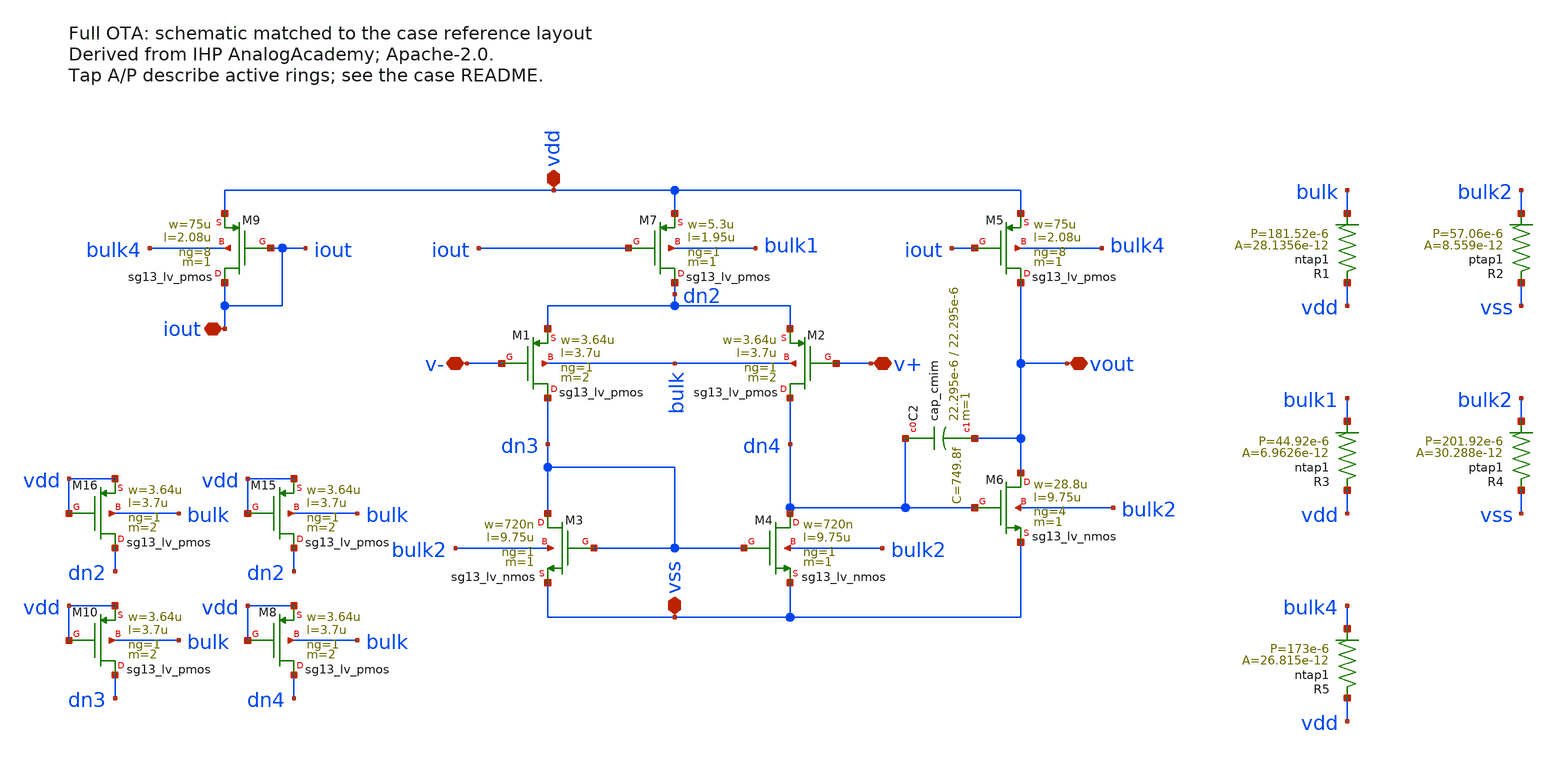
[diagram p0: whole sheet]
** sch_path: tasks/IHP-AnalogAcademy/cases/full_OTA/source/two_stage_OTA_layout.sch
**.subckt two_stage_OTA_layout v- v+ vss vdd iout vout
*.iopin v-
*.iopin v+
*.iopin vss
*.iopin vdd
*.iopin iout
*.iopin vout
XM4 dn4 dn3 vss bulk2 sg13_lv_nmos w=720n l=9.75u ng=1 m=1 mm_ok=1
XM3 dn3 dn3 vss bulk2 sg13_lv_nmos w=720n l=9.75u ng=1 m=1 mm_ok=1
XM1 dn3 v- dn2 bulk sg13_lv_pmos w=3.64u l=3.7u ng=1 m=2 mm_ok=1
XM2 dn4 v+ dn2 bulk sg13_lv_pmos w=3.64u l=3.7u ng=1 m=2 mm_ok=1
XM7 dn2 iout vdd bulk1 sg13_lv_pmos w=5.3u l=1.95u ng=1 m=1 mm_ok=1
XM5 vout iout vdd bulk4 sg13_lv_pmos w=75u l=2.08u ng=8 m=1 mm_ok=1
XM6 vout dn4 vss bulk2 sg13_lv_nmos w=28.8u l=9.75u ng=4 m=1 mm_ok=1
XM9 iout iout vdd bulk4 sg13_lv_pmos w=75u l=2.08u ng=8 m=1 mm_ok=1
XC2 dn4 vout cap_cmim w=22.295e-6 l=22.295e-6 m=1 mm_ok=1
XM8 dn4 vdd vdd bulk sg13_lv_pmos w=3.64u l=3.7u ng=1 m=2 mm_ok=1
XM10 dn3 vdd vdd bulk sg13_lv_pmos w=3.64u l=3.7u ng=1 m=2 mm_ok=1
XM15 dn2 vdd vdd bulk sg13_lv_pmos w=3.64u l=3.7u ng=1 m=2 mm_ok=1
XM16 dn2 vdd vdd bulk sg13_lv_pmos w=3.64u l=3.7u ng=1 m=2 mm_ok=1
XR1 vdd bulk ntap1 a=28.1356e-12 p=181.52e-6 r=4.674
XR3 vdd bulk1 ntap1 a=6.9626e-12 p=44.92e-6 r=18.89
XR5 vdd bulk4 ntap1 a=26.815e-12 p=173e-6 r=4.905
XR2 vss bulk2 ptap1 a=8.559e-12 p=57.06e-6 r=14.93
XR4 vss bulk2 ptap1 a=30.288e-12 p=201.92e-6 r=4.22
**.ends
.end
